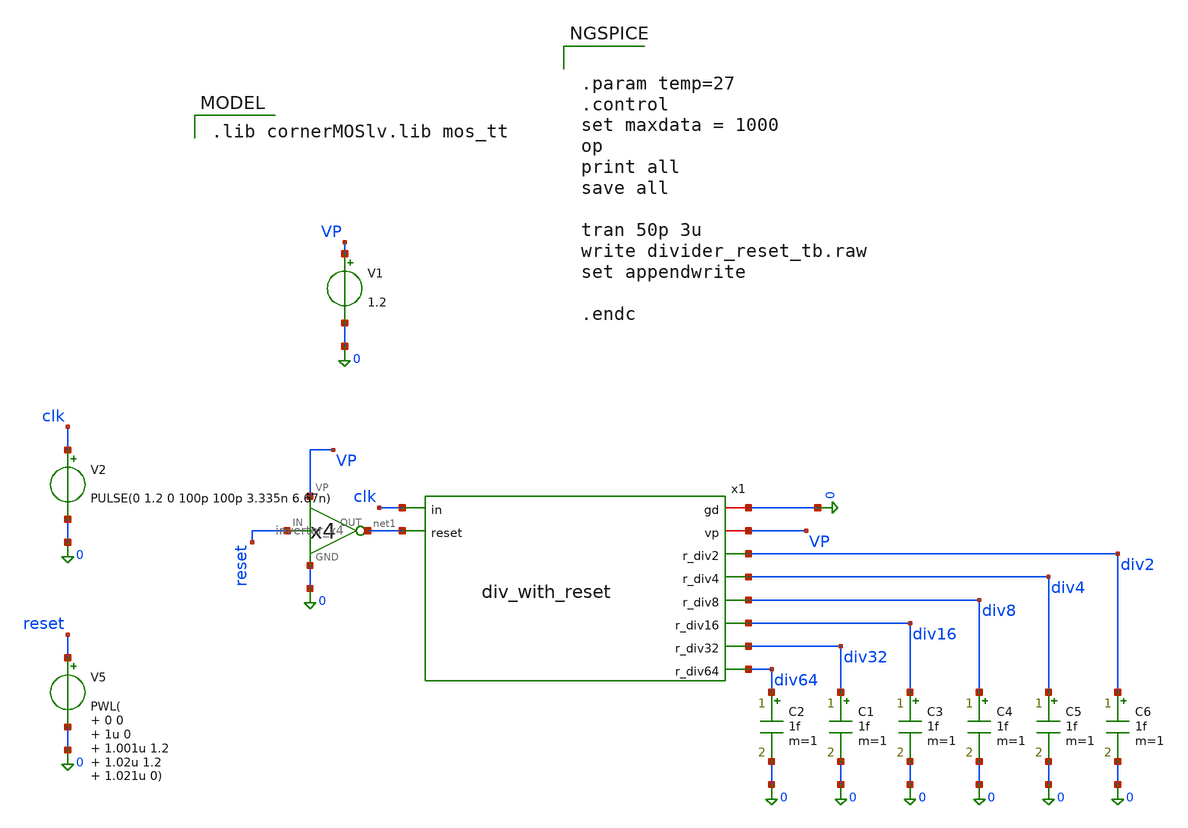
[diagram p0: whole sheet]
** sch_path: PLL0663-main/testbenches/tran/xschem/divider/divider_reset_tb.sch
**.subckt divider_reset_tb
V1 VP 0 1.2
V2 clk 0 PULSE(0 1.2 0 100p 100p 3.335n 6.67n)
C2 div64 0 1f m=1
V5 reset 0 PWL( 0 0 1u 0 1.001u 1.2 1.02u 1.2 1.021u 0)
C1 div32 0 1f m=1
C3 div16 0 1f m=1
C4 div8 0 1f m=1
C5 div4 0 1f m=1
C6 div2 0 1f m=1
x1 0 VP clk net1 div2 div4 div8 div16 div32 div64 div_with_reset
x8 reset net1 VP 0 inverter_x4
**** begin user architecture code
 .lib cornerMOSlv.lib mos_tt



.param temp=27
.control
set maxdata = 1000
op
print all
save all

tran 50p 3u
write divider_reset_tb.raw
set appendwrite

.endc


**** end user architecture code
**.ends
.end
